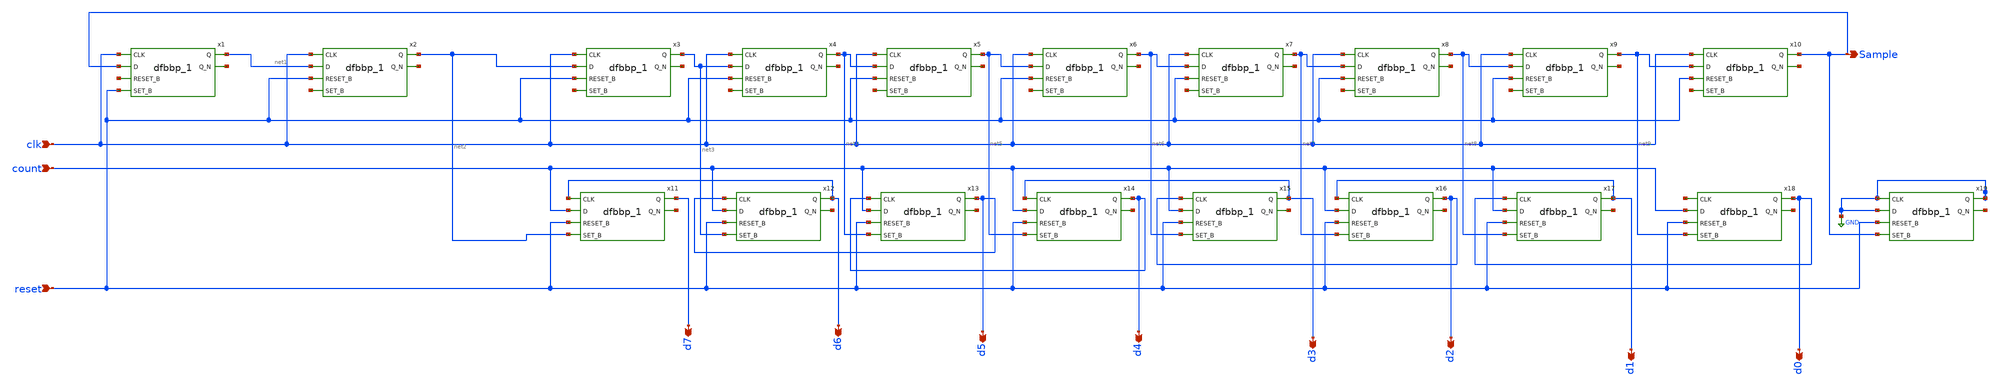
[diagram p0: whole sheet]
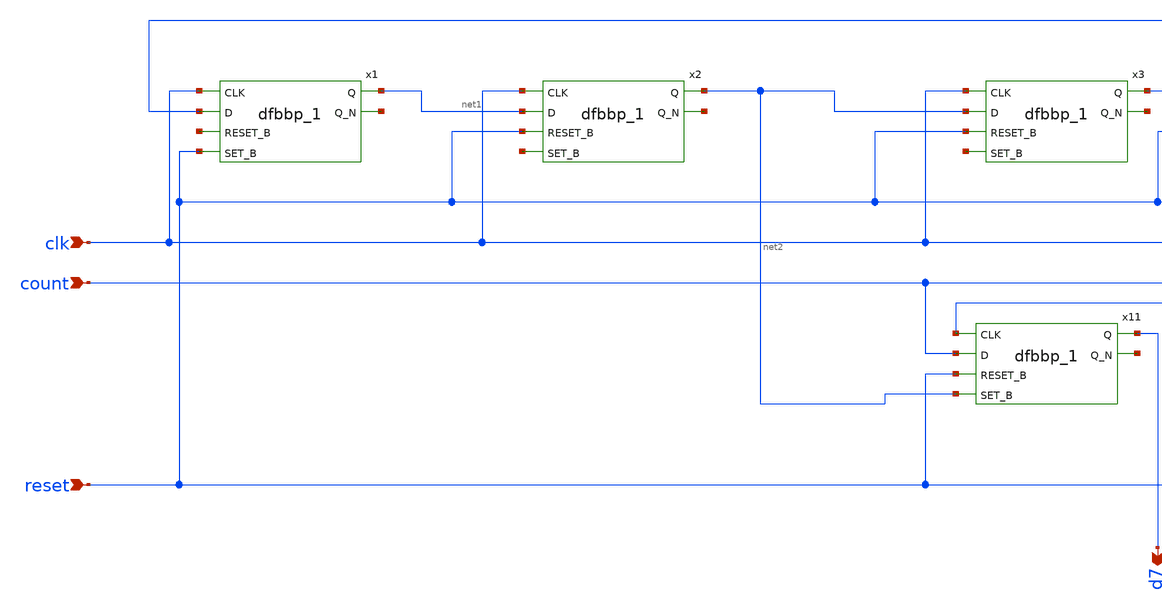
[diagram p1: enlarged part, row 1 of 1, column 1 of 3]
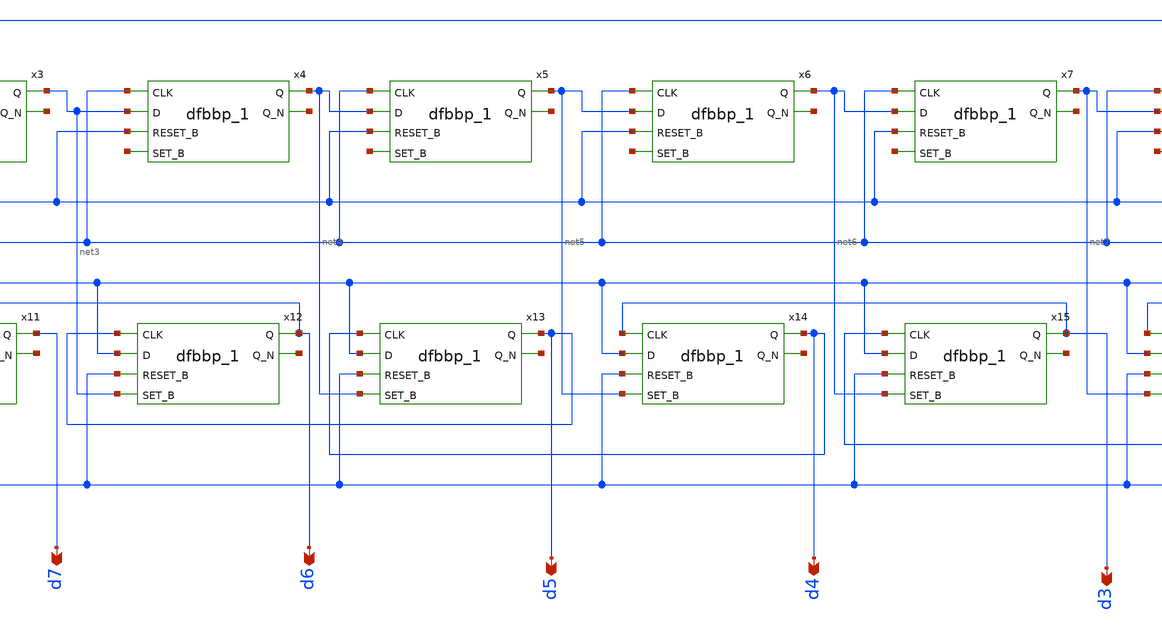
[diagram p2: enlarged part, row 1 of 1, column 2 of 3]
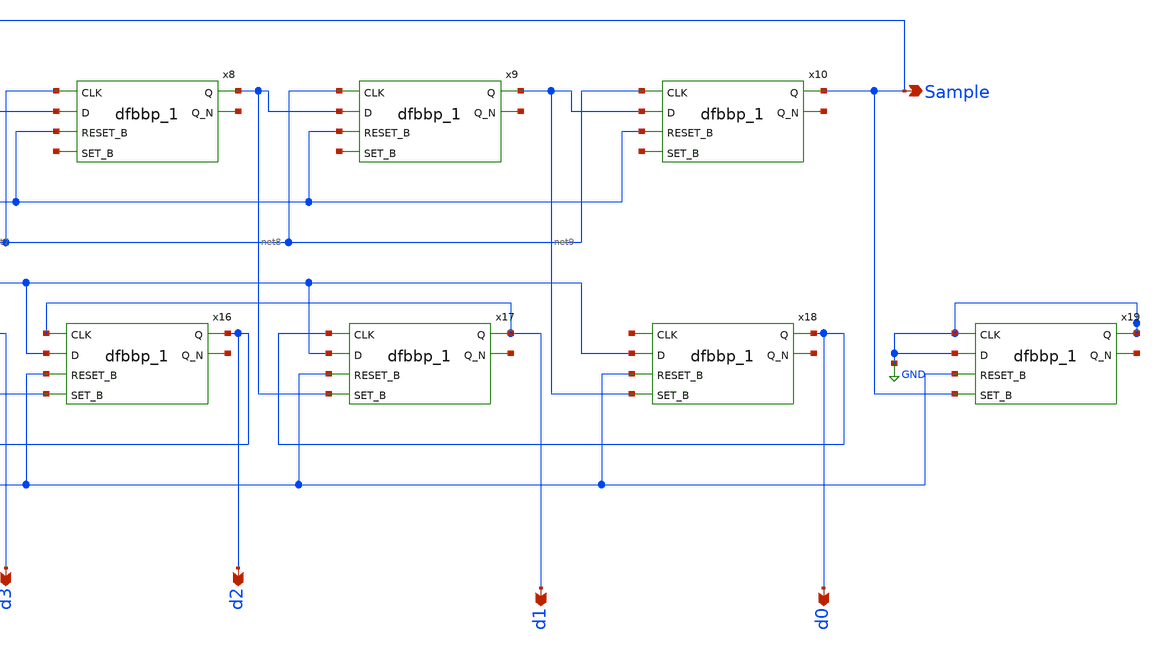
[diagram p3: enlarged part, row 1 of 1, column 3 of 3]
** sch_path: Behavioral_model/controller.sch
* Copyright 2022 Stefan Frederik Schippers
* Licensed under the Apache License, Version 2.0 (the "License");
* you may not use this file except in compliance with the License.
* You may obtain a copy of the License at
* https://www.apache.org/licenses/LICENSE-2.0
* Unless required by applicable law or agreed to in writing, software
* distributed under the License is distributed on an "AS IS" BASIS,
* WITHOUT WARRANTIES OR CONDITIONS OF ANY KIND, either express or implied.
* See the License for the specific language governing permissions and
* limitations under the License.
.lib $::SKYWATER_MODELS/sky130.lib.spice tt
.include $::SKYWATER_STDCELLS/sky130_fd_sc_hd.spice

**.subckt controller d0 d1 d2 d3 d4 d5 d6 d7 Sample clk count reset
*.opin d0
*.opin d1
*.opin d2
*.opin d3
*.opin d4
*.opin d5
*.opin d6
*.opin d7
*.opin Sample
*.ipin clk
*.ipin count
*.ipin reset
x1 clk Sample net10 reset vss vss vcc vcc net1 net11 sky130_fd_sc_hd__dfbbp_1
x2 clk net1 reset net12 vss vss vcc vcc net2 net13 sky130_fd_sc_hd__dfbbp_1
x3 clk net2 reset net14 vss vss vcc vcc net3 net15 sky130_fd_sc_hd__dfbbp_1
x4 clk net3 reset net16 vss vss vcc vcc net4 net17 sky130_fd_sc_hd__dfbbp_1
x5 clk net4 reset net18 vss vss vcc vcc net5 net19 sky130_fd_sc_hd__dfbbp_1
x6 clk net5 reset net20 vss vss vcc vcc net6 net21 sky130_fd_sc_hd__dfbbp_1
x7 clk net6 reset net22 vss vss vcc vcc net7 net23 sky130_fd_sc_hd__dfbbp_1
x8 clk net7 reset net24 vss vss vcc vcc net8 net25 sky130_fd_sc_hd__dfbbp_1
x9 clk net8 reset net26 vss vss vcc vcc net9 net27 sky130_fd_sc_hd__dfbbp_1
x10 clk net9 reset net28 vss vss vcc vcc Sample net29 sky130_fd_sc_hd__dfbbp_1
x11 d6 count reset net2 vss vss vcc vcc d7 net30 sky130_fd_sc_hd__dfbbp_1
x12 d5 count reset net3 vss vss vcc vcc d6 net31 sky130_fd_sc_hd__dfbbp_1
x13 d4 count reset net4 vss vss vcc vcc d5 net32 sky130_fd_sc_hd__dfbbp_1
x14 d3 count reset net5 vss vss vcc vcc d4 net33 sky130_fd_sc_hd__dfbbp_1
x15 d2 count reset net6 vss vss vcc vcc d3 net34 sky130_fd_sc_hd__dfbbp_1
x16 d1 count reset net7 vss vss vcc vcc d2 net35 sky130_fd_sc_hd__dfbbp_1
x17 d0 count reset net8 vss vss vcc vcc d1 net36 sky130_fd_sc_hd__dfbbp_1
x18 net37 count reset net9 vss vss vcc vcc d0 net38 sky130_fd_sc_hd__dfbbp_1
x19 GND GND reset Sample vss vss vcc vcc GND net39 sky130_fd_sc_hd__dfbbp_1
**.ends
.GLOBAL GND
.end
